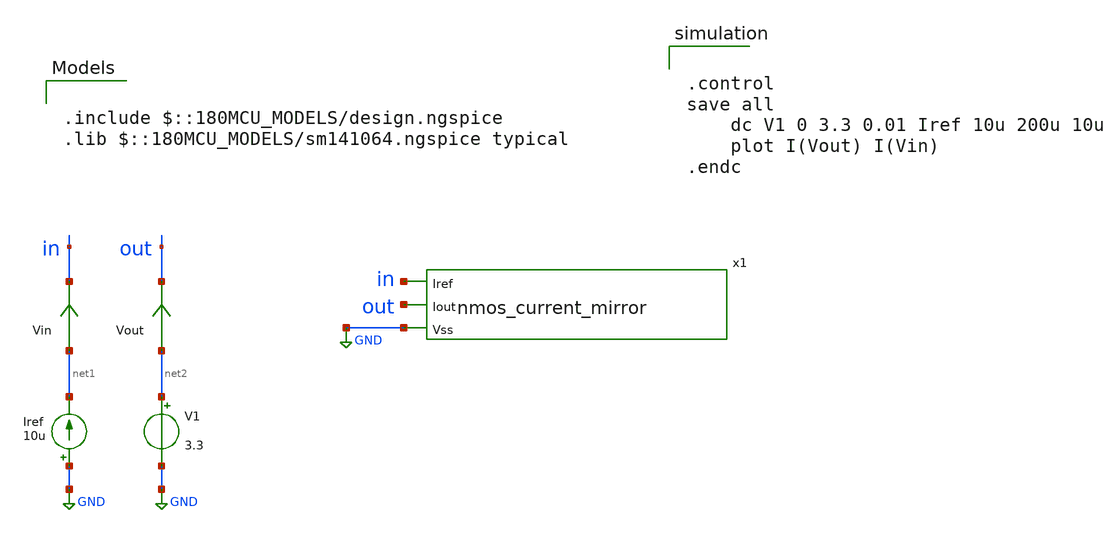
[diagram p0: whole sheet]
** sch_path: designs/libs/tb_current-mirror/tb_nmos_current_mirror/tb_nmos_current_mirror.sch
**.subckt tb_nmos_current_mirror
Iref GND net1 10u
V1 net2 GND 3.3
Vin net1 in 0
.save i(vin)
Vout net2 out 0
.save i(vout)
x1 in out GND nmos_current_mirror
**** begin user architecture code


.control
save all
	dc V1 0 3.3 0.01 Iref 10u 200u 10u
	plot I(Vout) I(Vin)
.endc



.include $::180MCU_MODELS/design.ngspice
.lib $::180MCU_MODELS/sm141064.ngspice typical

**** end user architecture code
**.ends
.GLOBAL GND
.end
